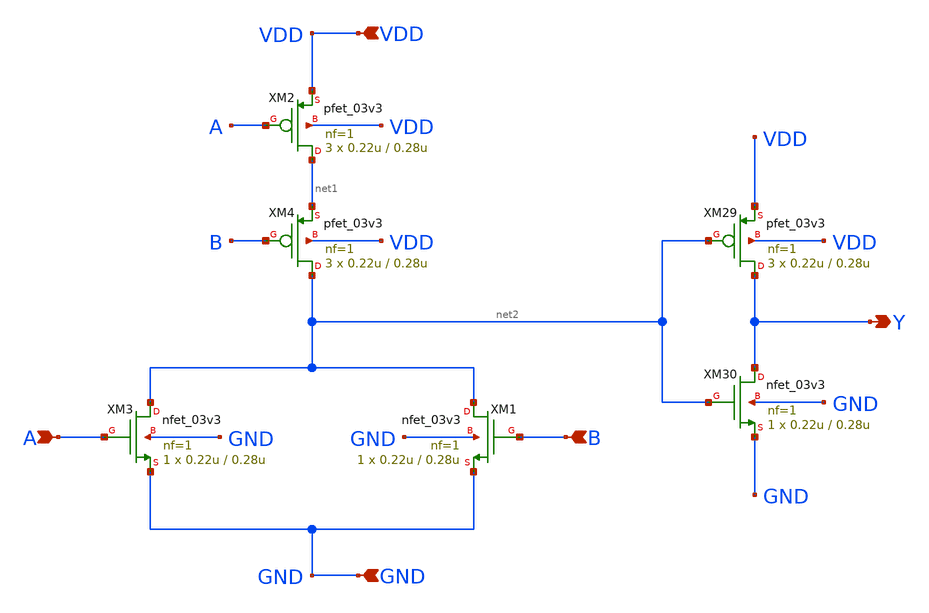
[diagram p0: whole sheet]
** sch_path: PFD/OR.sch
**.subckt OR Y GND VDD A B
*.opin Y
*.ipin GND
*.ipin VDD
*.ipin A
*.ipin B
XM3 net2 A GND GND nfet_03v3 L=0.28u W=0.22u nf=1 ad='int((nf+1)/2) * W/nf * 0.18u' as='int((nf+2)/2) * W/nf * 0.18u'
+ pd='2*int((nf+1)/2) * (W/nf + 0.18u)' ps='2*int((nf+2)/2) * (W/nf + 0.18u)' nrd='0.18u / W' nrs='0.18u / W'
+ sa=0 sb=0 sd=0 m=1
XM2 net1 A VDD VDD pfet_03v3 L=0.28u W=0.22u nf=1 ad='int((nf+1)/2) * W/nf * 0.18u' as='int((nf+2)/2) * W/nf * 0.18u'
+ pd='2*int((nf+1)/2) * (W/nf + 0.18u)' ps='2*int((nf+2)/2) * (W/nf + 0.18u)' nrd='0.18u / W' nrs='0.18u / W'
+ sa=0 sb=0 sd=0 m=3
XM4 net2 B net1 VDD pfet_03v3 L=0.28u W=0.22u nf=1 ad='int((nf+1)/2) * W/nf * 0.18u' as='int((nf+2)/2) * W/nf * 0.18u'
+ pd='2*int((nf+1)/2) * (W/nf + 0.18u)' ps='2*int((nf+2)/2) * (W/nf + 0.18u)' nrd='0.18u / W' nrs='0.18u / W'
+ sa=0 sb=0 sd=0 m=3
XM1 net2 B GND GND nfet_03v3 L=0.28u W=0.22u nf=1 ad='int((nf+1)/2) * W/nf * 0.18u' as='int((nf+2)/2) * W/nf * 0.18u'
+ pd='2*int((nf+1)/2) * (W/nf + 0.18u)' ps='2*int((nf+2)/2) * (W/nf + 0.18u)' nrd='0.18u / W' nrs='0.18u / W'
+ sa=0 sb=0 sd=0 m=1
XM29 Y net2 VDD VDD pfet_03v3 L=0.28u W=0.22u nf=1 ad='int((nf+1)/2) * W/nf * 0.18u' as='int((nf+2)/2) * W/nf * 0.18u'
+ pd='2*int((nf+1)/2) * (W/nf + 0.18u)' ps='2*int((nf+2)/2) * (W/nf + 0.18u)' nrd='0.18u / W' nrs='0.18u / W'
+ sa=0 sb=0 sd=0 m=3
XM30 Y net2 GND GND nfet_03v3 L=0.28u W=0.22u nf=1 ad='int((nf+1)/2) * W/nf * 0.18u' as='int((nf+2)/2) * W/nf * 0.18u'
+ pd='2*int((nf+1)/2) * (W/nf + 0.18u)' ps='2*int((nf+2)/2) * (W/nf + 0.18u)' nrd='0.18u / W' nrs='0.18u / W'
+ sa=0 sb=0 sd=0 m=1
**.ends
.end
